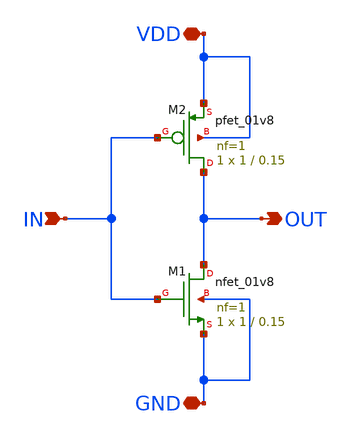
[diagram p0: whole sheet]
** sch_path: ring_oscillator/inverter.sch
**.subckt inverter IN VDD GND OUT
*.ipin IN
*.iopin VDD
*.iopin GND
*.opin OUT
XM1 OUT IN GND GND sky130_fd_pr__nfet_01v8 L=0.15 W=1 nf=1 ad='int((nf+1)/2) * W/nf * 0.29' as='int((nf+2)/2) * W/nf * 0.29'
+ pd='2*int((nf+1)/2) * (W/nf + 0.29)' ps='2*int((nf+2)/2) * (W/nf + 0.29)' nrd='0.29 / W' nrs='0.29 / W'
+ sa=0 sb=0 sd=0 mult=1 m=1
XM2 OUT IN VDD VDD sky130_fd_pr__pfet_01v8 L=0.15 W=1 nf=1 ad='int((nf+1)/2) * W/nf * 0.29' as='int((nf+2)/2) * W/nf * 0.29'
+ pd='2*int((nf+1)/2) * (W/nf + 0.29)' ps='2*int((nf+2)/2) * (W/nf + 0.29)' nrd='0.29 / W' nrs='0.29 / W'
+ sa=0 sb=0 sd=0 mult=1 m=1
**.ends
.end
